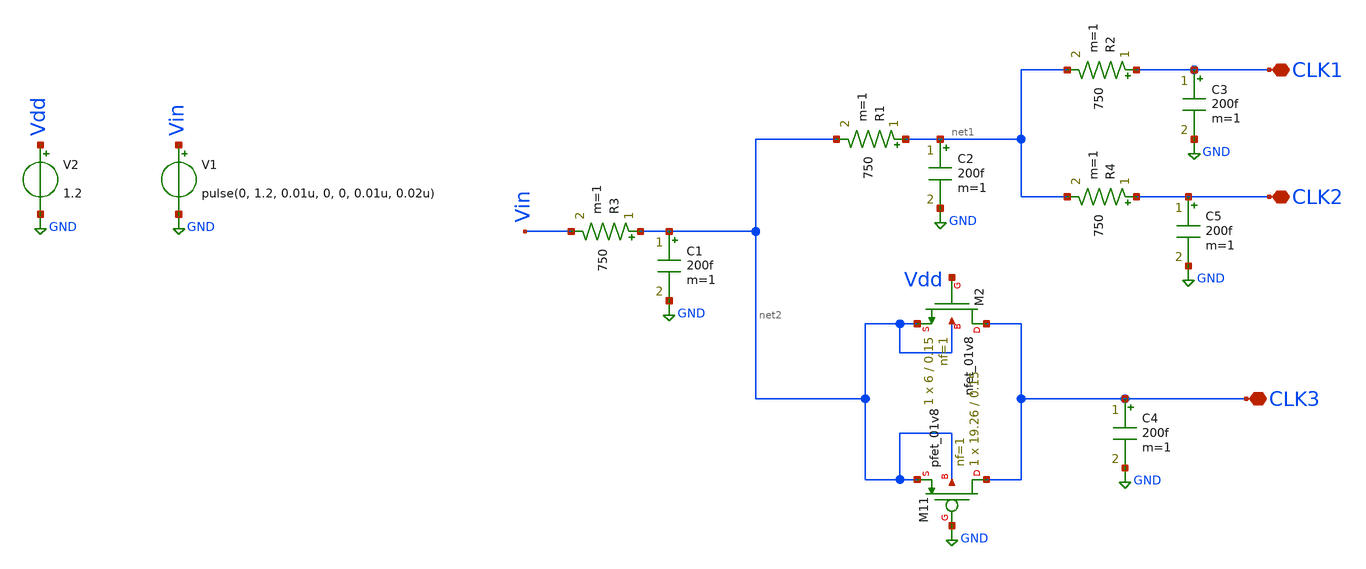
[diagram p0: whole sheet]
** sch_path: HW-4/hw-4.sch
**.subckt hw-4 CLK1 CLK2 CLK3
*.iopin CLK1
*.iopin CLK2
*.iopin CLK3
R1 net1 net2 750 m=1
R2 CLK1 net1 750 m=1
R3 net2 Vin 750 m=1
R4 CLK2 net1 750 m=1
C1 net2 GND 200f m=1
C2 net1 GND 200f m=1
C3 CLK1 GND 200f m=1
C4 CLK3 GND 200f m=1
XM2 CLK3 Vdd net2 net2 sky130_fd_pr__nfet_01v8 L=0.15 W=6 nf=1 ad='int((1 + 1)/2) * 6 / 1 * 0.29' as='int((1 + 2)/2) * 6 / 1 * 0.29'
+ pd='2*int((1 + 1)/2) * (6 / 1 + 0.29)' ps='2*int((1 + 2)/2) * (6 / 1 + 0.29)' nrd='0.29 / 6 ' nrs='0.29 / 6 '
+ sa=0 sb=0 sd=0 mult=1 m=1
XM11 CLK3 GND net2 net2 sky130_fd_pr__pfet_01v8 L=0.15 W=19.26 nf=1 ad='int((nf+1)/2) * W/nf * 0.29'
+ as='int((nf+2)/2) * W/nf * 0.29' pd='2*int((nf+1)/2) * (W/nf + 0.29)' ps='2*int((nf+2)/2) * (W/nf + 0.29)'
+ nrd='0.29 / W' nrs='0.29 / W' sa=0 sb=0 sd=0 mult=1 m=1
V1 Vin GND pulse(0, 1.2, 0.01u, 0, 0, 0.01u, 0.02u)
V2 Vdd GND 1.2
C5 CLK2 GND 200f m=1
**** begin user architecture code

** opencircuitdesign pdks install
.lib $::SKYWATER_MODELS/sky130.lib.spice tt




.control
set color0 = white

save all
tran 0.001n 0.03u

plot Vin CLK1 CLK2 CLK3

.endc


**** end user architecture code
**.ends
.GLOBAL GND
.end
